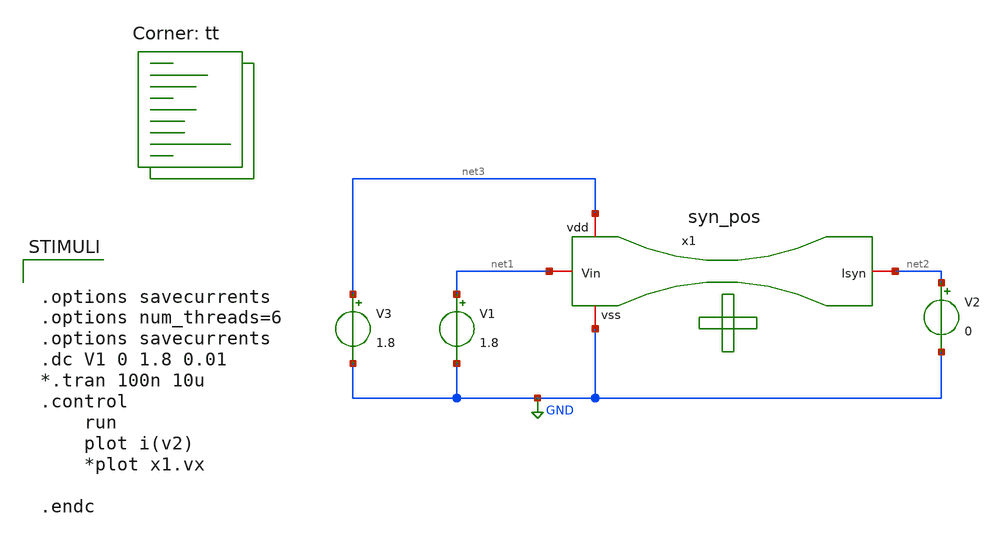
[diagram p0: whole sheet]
** sch_path: Neuron/ultralif/tb_syn_pos.sch
**.subckt tb_syn_pos
x1 GND net1 net2 net3 syn_pos
V1 net1 GND 1.8
V2 net2 GND 0
V3 net3 GND 1.8
**** begin user architecture code
.lib $::SKYWATER_MODELS/sky130.lib.spice tt
**** end user architecture code
**.ends

* expanding   symbol:  syn_pos.sym # of pins=4
** sym_path: Neuron/ultralif/syn_pos.sym
** sch_path: Neuron/ultralif/syn_pos.sch
.subckt syn_pos vss Vin Isyn vdd
*.iopin Vin
*.iopin vdd
*.iopin vss
*.iopin Isyn
XM9 Isyn vx vdd vdd sky130_fd_pr__pfet_01v8 L=1 W=0.5 nf=1 ad='int((nf+1)/2) * W/nf * 0.29' as='int((nf+2)/2) * W/nf * 0.29'
+ pd='2*int((nf+1)/2) * (W/nf + 0.29)' ps='2*int((nf+2)/2) * (W/nf + 0.29)' nrd='0.29 / W' nrs='0.29 / W'
+ sa=0 sb=0 sd=0 mult=1 m=1
XM10 vx vx vdd vdd sky130_fd_pr__pfet_01v8 L=0.15 W=0.5 nf=1 ad='int((nf+1)/2) * W/nf * 0.29' as='int((nf+2)/2) * W/nf * 0.29'
+ pd='2*int((nf+1)/2) * (W/nf + 0.29)' ps='2*int((nf+2)/2) * (W/nf + 0.29)' nrd='0.29 / W' nrs='0.29 / W'
+ sa=0 sb=0 sd=0 mult=5 m=5
XM12 vx Vin vss vss sky130_fd_pr__nfet_01v8 L=1 W=0.4 nf=1 ad='int((1 + 1)/2) * 0.4 / 1 * 0.29' as='int((1 + 2)/2) * 0.4 / 1 * 0.29'
+ pd='2*int((1 + 1)/2) * (0.4 / 1 + 0.29)' ps='2*int((1 + 2)/2) * (0.4 / 1 + 0.29)' nrd='0.29 / 0.4 ' nrs='0.29 / 0.4 '
+ sa=0 sb=0 sd=0 mult=1 m=1
.ends

.GLOBAL GND
**** begin user architecture code


.options savecurrents
.options num_threads=6
.options savecurrents
.dc V1 0 1.8 0.01
*.tran 100n 10u
.control
	run
	plot i(v2)
	*plot x1.vx

.endc


**** end user architecture code
.end
